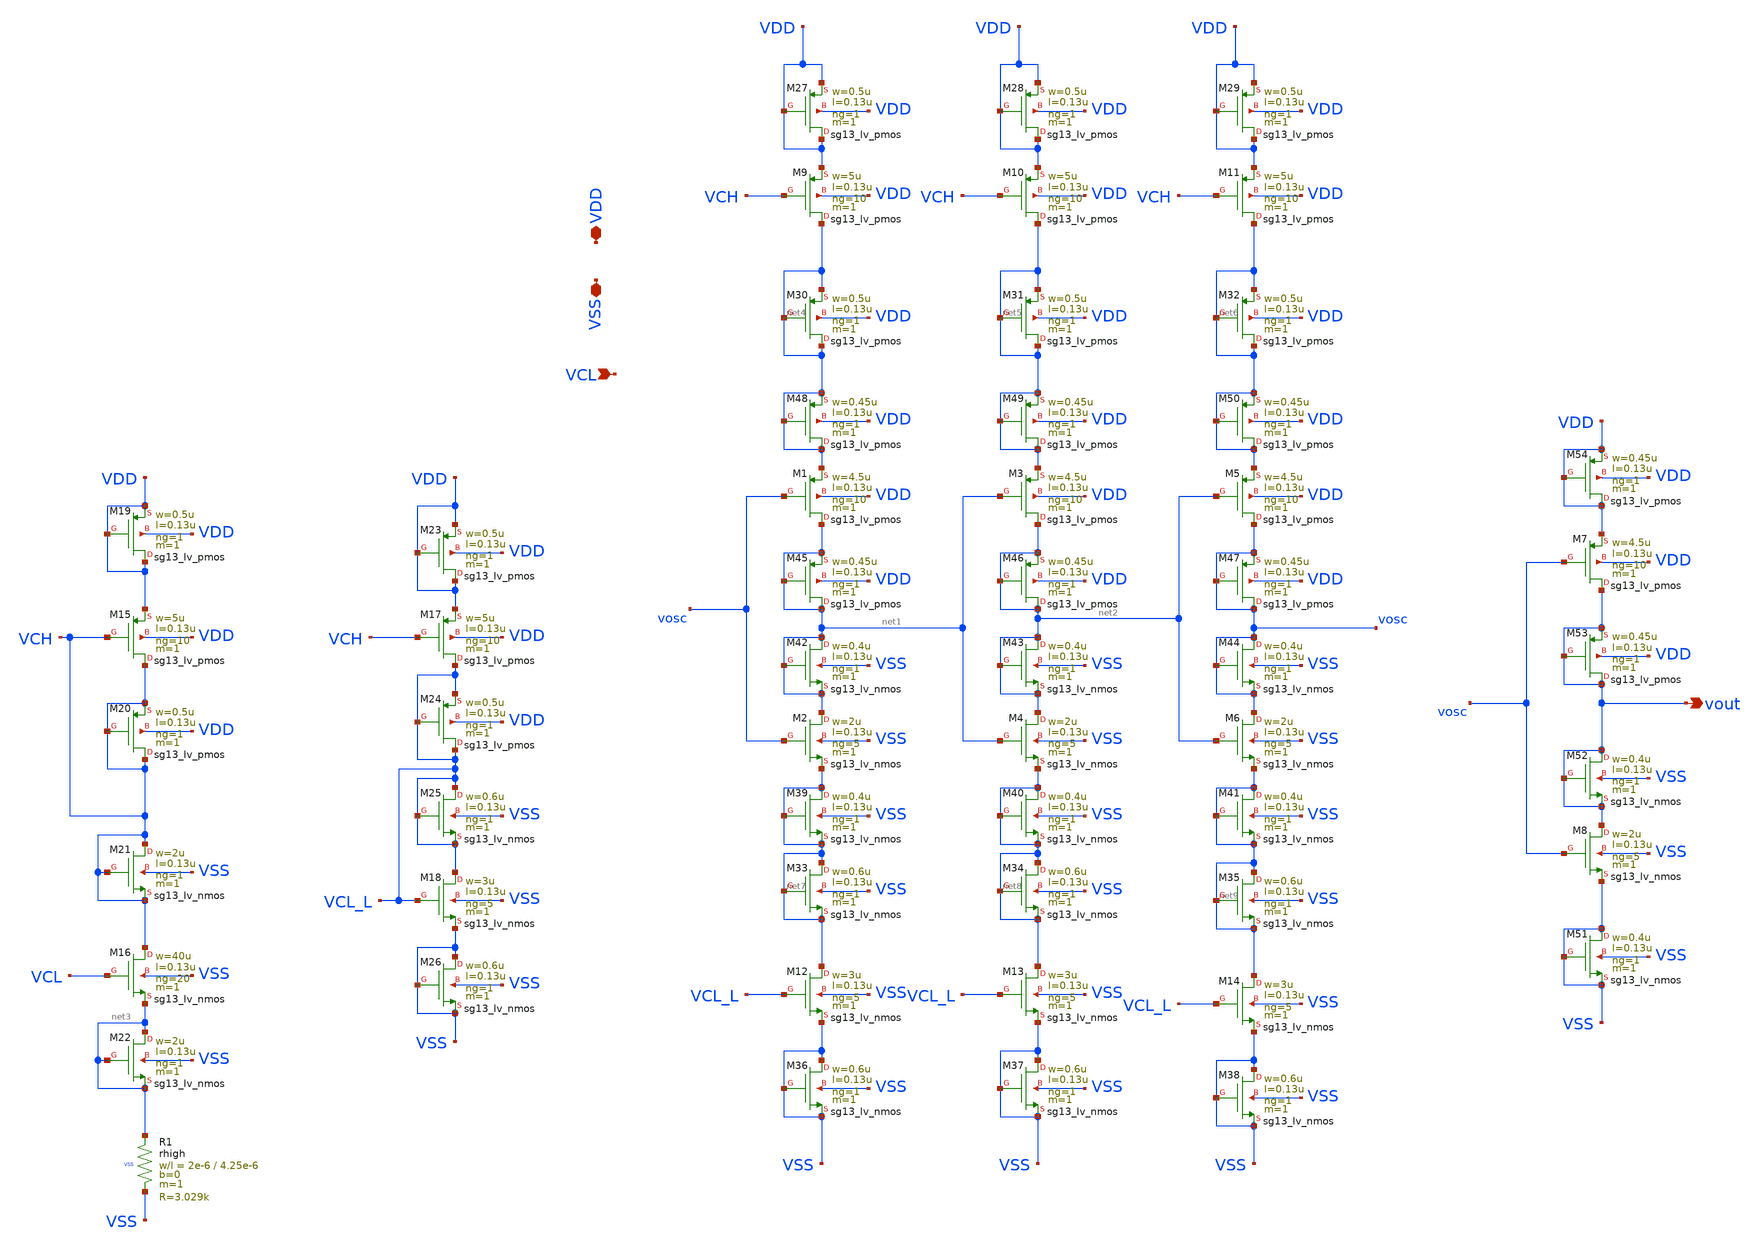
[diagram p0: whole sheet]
** sch_path: macros/heichips26_ook/macros/ook_analog_system/schematic/xschem/vco.sch
**.subckt vco vout VDD VSS VCL
*.opin vout
*.iopin VDD
*.iopin VSS
*.ipin VCL
XM1 net1 vosc net4 VDD sg13_lv_pmos w=4.5u l=0.13u ng=10 m=1 mm_ok=1
XM2 net1 vosc net7 VSS sg13_lv_nmos w=2u l=0.13u ng=5 m=1 mm_ok=1
XM3 net2 net1 net5 VDD sg13_lv_pmos w=4.5u l=0.13u ng=10 m=1 mm_ok=1
XM4 net2 net1 net8 VSS sg13_lv_nmos w=2u l=0.13u ng=5 m=1 mm_ok=1
XM5 vosc net2 net6 VDD sg13_lv_pmos w=4.5u l=0.13u ng=10 m=1 mm_ok=1
XM6 vosc net2 net9 VSS sg13_lv_nmos w=2u l=0.13u ng=5 m=1 mm_ok=1
XM7 vout vosc VDD VDD sg13_lv_pmos w=4.5u l=0.13u ng=10 m=1 mm_ok=1
XM8 vout vosc VSS VSS sg13_lv_nmos w=2u l=0.13u ng=5 m=1 mm_ok=1
XM9 net4 VCH VDD VDD sg13_lv_pmos w=5u l=0.13u ng=10 m=1 mm_ok=1
XM10 net5 VCH VDD VDD sg13_lv_pmos w=5u l=0.13u ng=10 m=1 mm_ok=1
XM11 net6 VCH VDD VDD sg13_lv_pmos w=5u l=0.13u ng=10 m=1 mm_ok=1
XM12 net7 VCL_L VSS VSS sg13_lv_nmos w=3u l=0.13u ng=5 m=1 mm_ok=1
XM13 net8 VCL_L VSS VSS sg13_lv_nmos w=3u l=0.13u ng=5 m=1 mm_ok=1
XM14 net9 VCL_L VSS VSS sg13_lv_nmos w=3u l=0.13u ng=5 m=1 mm_ok=1
XM15 VCH VCH VDD VDD sg13_lv_pmos w=5u l=0.13u ng=10 m=1 mm_ok=1
XM16 VCH VCL net3 VSS sg13_lv_nmos w=40u l=0.13u ng=20 m=1 mm_ok=1
XM17 VCL_L VCH VDD VDD sg13_lv_pmos w=5u l=0.13u ng=10 m=1 mm_ok=1
XM18 VCL_L VCL_L VSS VSS sg13_lv_nmos w=3u l=0.13u ng=5 m=1 mm_ok=1
XR1 net3 VSS VSS rhigh w=2e-6 l=4.25e-6 m=1 b=0 mm_ok=1
XM19 VDD VDD VDD VDD sg13_lv_pmos w=0.5u l=0.13u ng=1 m=1 mm_ok=1
XM20 VCH VCH VCH VDD sg13_lv_pmos w=0.5u l=0.13u ng=1 m=1 mm_ok=1
XM21 VCH VCH VCH VSS sg13_lv_nmos w=2u l=0.13u ng=1 m=1 mm_ok=1
XM22 net3 net3 net3 VSS sg13_lv_nmos w=2u l=0.13u ng=1 m=1 mm_ok=1
XM23 VDD VDD VDD VDD sg13_lv_pmos w=0.5u l=0.13u ng=1 m=1 mm_ok=1
XM24 VCL_L VCL_L VCL_L VDD sg13_lv_pmos w=0.5u l=0.13u ng=1 m=1 mm_ok=1
XM25 VCL_L VCL_L VCL_L VSS sg13_lv_nmos w=0.6u l=0.13u ng=1 m=1 mm_ok=1
XM26 VSS VSS VSS VSS sg13_lv_nmos w=0.6u l=0.13u ng=1 m=1 mm_ok=1
XM27 VDD VDD VDD VDD sg13_lv_pmos w=0.5u l=0.13u ng=1 m=1 mm_ok=1
XM28 VDD VDD VDD VDD sg13_lv_pmos w=0.5u l=0.13u ng=1 m=1 mm_ok=1
XM29 VDD VDD VDD VDD sg13_lv_pmos w=0.5u l=0.13u ng=1 m=1 mm_ok=1
XM30 net4 net4 net4 VDD sg13_lv_pmos w=0.5u l=0.13u ng=1 m=1 mm_ok=1
XM31 net5 net5 net5 VDD sg13_lv_pmos w=0.5u l=0.13u ng=1 m=1 mm_ok=1
XM32 net6 net6 net6 VDD sg13_lv_pmos w=0.5u l=0.13u ng=1 m=1 mm_ok=1
XM33 net7 net7 net7 VSS sg13_lv_nmos w=0.6u l=0.13u ng=1 m=1 mm_ok=1
XM34 net8 net8 net8 VSS sg13_lv_nmos w=0.6u l=0.13u ng=1 m=1 mm_ok=1
XM35 net9 net9 net9 VSS sg13_lv_nmos w=0.6u l=0.13u ng=1 m=1 mm_ok=1
XM36 VSS VSS VSS VSS sg13_lv_nmos w=0.6u l=0.13u ng=1 m=1 mm_ok=1
XM37 VSS VSS VSS VSS sg13_lv_nmos w=0.6u l=0.13u ng=1 m=1 mm_ok=1
XM38 VSS VSS VSS VSS sg13_lv_nmos w=0.6u l=0.13u ng=1 m=1 mm_ok=1
XM39 net7 net7 net7 VSS sg13_lv_nmos w=0.4u l=0.13u ng=1 m=1 mm_ok=1
XM40 net8 net8 net8 VSS sg13_lv_nmos w=0.4u l=0.13u ng=1 m=1 mm_ok=1
XM41 net9 net9 net9 VSS sg13_lv_nmos w=0.4u l=0.13u ng=1 m=1 mm_ok=1
XM42 net1 net1 net1 VSS sg13_lv_nmos w=0.4u l=0.13u ng=1 m=1 mm_ok=1
XM43 net2 net2 net2 VSS sg13_lv_nmos w=0.4u l=0.13u ng=1 m=1 mm_ok=1
XM44 vosc vosc vosc VSS sg13_lv_nmos w=0.4u l=0.13u ng=1 m=1 mm_ok=1
XM45 net1 net1 net1 VDD sg13_lv_pmos w=0.45u l=0.13u ng=1 m=1 mm_ok=1
XM46 net2 net2 net2 VDD sg13_lv_pmos w=0.45u l=0.13u ng=1 m=1 mm_ok=1
XM47 vosc vosc vosc VDD sg13_lv_pmos w=0.45u l=0.13u ng=1 m=1 mm_ok=1
XM48 net4 net4 net4 VDD sg13_lv_pmos w=0.45u l=0.13u ng=1 m=1 mm_ok=1
XM49 net5 net5 net5 VDD sg13_lv_pmos w=0.45u l=0.13u ng=1 m=1 mm_ok=1
XM50 net6 net6 net6 VDD sg13_lv_pmos w=0.45u l=0.13u ng=1 m=1 mm_ok=1
XM51 VSS VSS VSS VSS sg13_lv_nmos w=0.4u l=0.13u ng=1 m=1 mm_ok=1
XM52 vout vout vout VSS sg13_lv_nmos w=0.4u l=0.13u ng=1 m=1 mm_ok=1
XM53 vout vout vout VDD sg13_lv_pmos w=0.45u l=0.13u ng=1 m=1 mm_ok=1
XM54 VDD VDD VDD VDD sg13_lv_pmos w=0.45u l=0.13u ng=1 m=1 mm_ok=1
**.ends
.end
